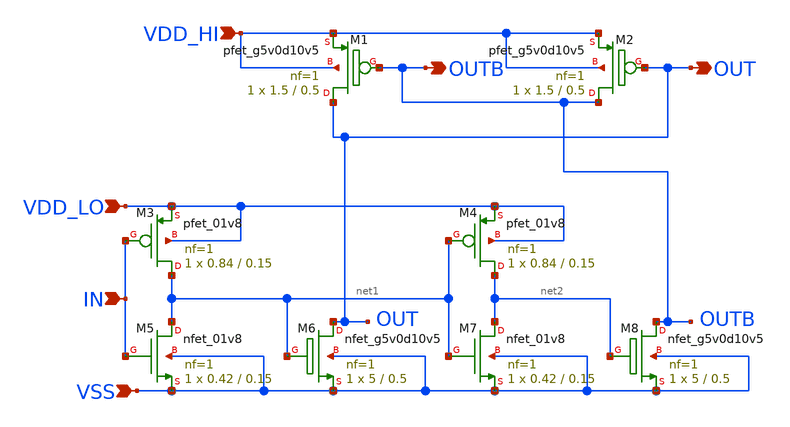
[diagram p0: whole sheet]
** sch_path: BL_SL_Writing_Interface/lvl_shifter_1p8_to_5.sch
**.subckt lvl_shifter_1p8_to_5 VDD_HI OUT OUTB IN VDD_LO VSS
*.ipin VDD_HI
*.opin OUT
*.opin OUTB
*.ipin IN
*.ipin VDD_LO
*.ipin VSS
XM5 net1 IN VSS VSS sky130_fd_pr__nfet_01v8 L=0.15 W=0.42 nf=1 ad='int((nf+1)/2) * W/nf * 0.29' as='int((nf+2)/2) * W/nf * 0.29'
+ pd='2*int((nf+1)/2) * (W/nf + 0.29)' ps='2*int((nf+2)/2) * (W/nf + 0.29)' nrd='0.29 / W' nrs='0.29 / W'
+ sa=0 sb=0 sd=0 mult=1 m=1
XM7 net2 net1 VSS VSS sky130_fd_pr__nfet_01v8 L=0.15 W=0.42 nf=1 ad='int((nf+1)/2) * W/nf * 0.29' as='int((nf+2)/2) * W/nf * 0.29'
+ pd='2*int((nf+1)/2) * (W/nf + 0.29)' ps='2*int((nf+2)/2) * (W/nf + 0.29)' nrd='0.29 / W' nrs='0.29 / W'
+ sa=0 sb=0 sd=0 mult=1 m=1
XM3 net1 IN VDD_LO VDD_LO sky130_fd_pr__pfet_01v8 L=0.15 W=0.84 nf=1 ad='int((nf+1)/2) * W/nf * 0.29'
+ as='int((nf+2)/2) * W/nf * 0.29' pd='2*int((nf+1)/2) * (W/nf + 0.29)' ps='2*int((nf+2)/2) * (W/nf + 0.29)'
+ nrd='0.29 / W' nrs='0.29 / W' sa=0 sb=0 sd=0 mult=1 m=1
XM4 net2 net1 VDD_LO VDD_LO sky130_fd_pr__pfet_01v8 L=0.15 W=0.84 nf=1 ad='int((nf+1)/2) * W/nf * 0.29'
+ as='int((nf+2)/2) * W/nf * 0.29' pd='2*int((nf+1)/2) * (W/nf + 0.29)' ps='2*int((nf+2)/2) * (W/nf + 0.29)'
+ nrd='0.29 / W' nrs='0.29 / W' sa=0 sb=0 sd=0 mult=1 m=1
XM6 OUT net1 VSS VSS sky130_fd_pr__nfet_g5v0d10v5 L=0.5 W=5 nf=1 ad='int((nf+1)/2) * W/nf * 0.29' as='int((nf+2)/2) * W/nf * 0.29'
+ pd='2*int((nf+1)/2) * (W/nf + 0.29)' ps='2*int((nf+2)/2) * (W/nf + 0.29)' nrd='0.29 / W' nrs='0.29 / W'
+ sa=0 sb=0 sd=0 mult=1 m=1
XM8 OUTB net2 VSS VSS sky130_fd_pr__nfet_g5v0d10v5 L=0.5 W=5 nf=1 ad='int((nf+1)/2) * W/nf * 0.29' as='int((nf+2)/2) * W/nf * 0.29'
+ pd='2*int((nf+1)/2) * (W/nf + 0.29)' ps='2*int((nf+2)/2) * (W/nf + 0.29)' nrd='0.29 / W' nrs='0.29 / W'
+ sa=0 sb=0 sd=0 mult=1 m=1
XM1 OUT OUTB VDD_HI VDD_HI sky130_fd_pr__pfet_g5v0d10v5 L=0.5 W=1.5 nf=1 ad='int((nf+1)/2) * W/nf * 0.29'
+ as='int((nf+2)/2) * W/nf * 0.29' pd='2*int((nf+1)/2) * (W/nf + 0.29)' ps='2*int((nf+2)/2) * (W/nf + 0.29)'
+ nrd='0.29 / W' nrs='0.29 / W' sa=0 sb=0 sd=0 mult=1 m=1
XM2 OUTB OUT VDD_HI VDD_HI sky130_fd_pr__pfet_g5v0d10v5 L=0.5 W=1.5 nf=1 ad='int((nf+1)/2) * W/nf * 0.29'
+ as='int((nf+2)/2) * W/nf * 0.29' pd='2*int((nf+1)/2) * (W/nf + 0.29)' ps='2*int((nf+2)/2) * (W/nf + 0.29)'
+ nrd='0.29 / W' nrs='0.29 / W' sa=0 sb=0 sd=0 mult=1 m=1
**.ends
.end
